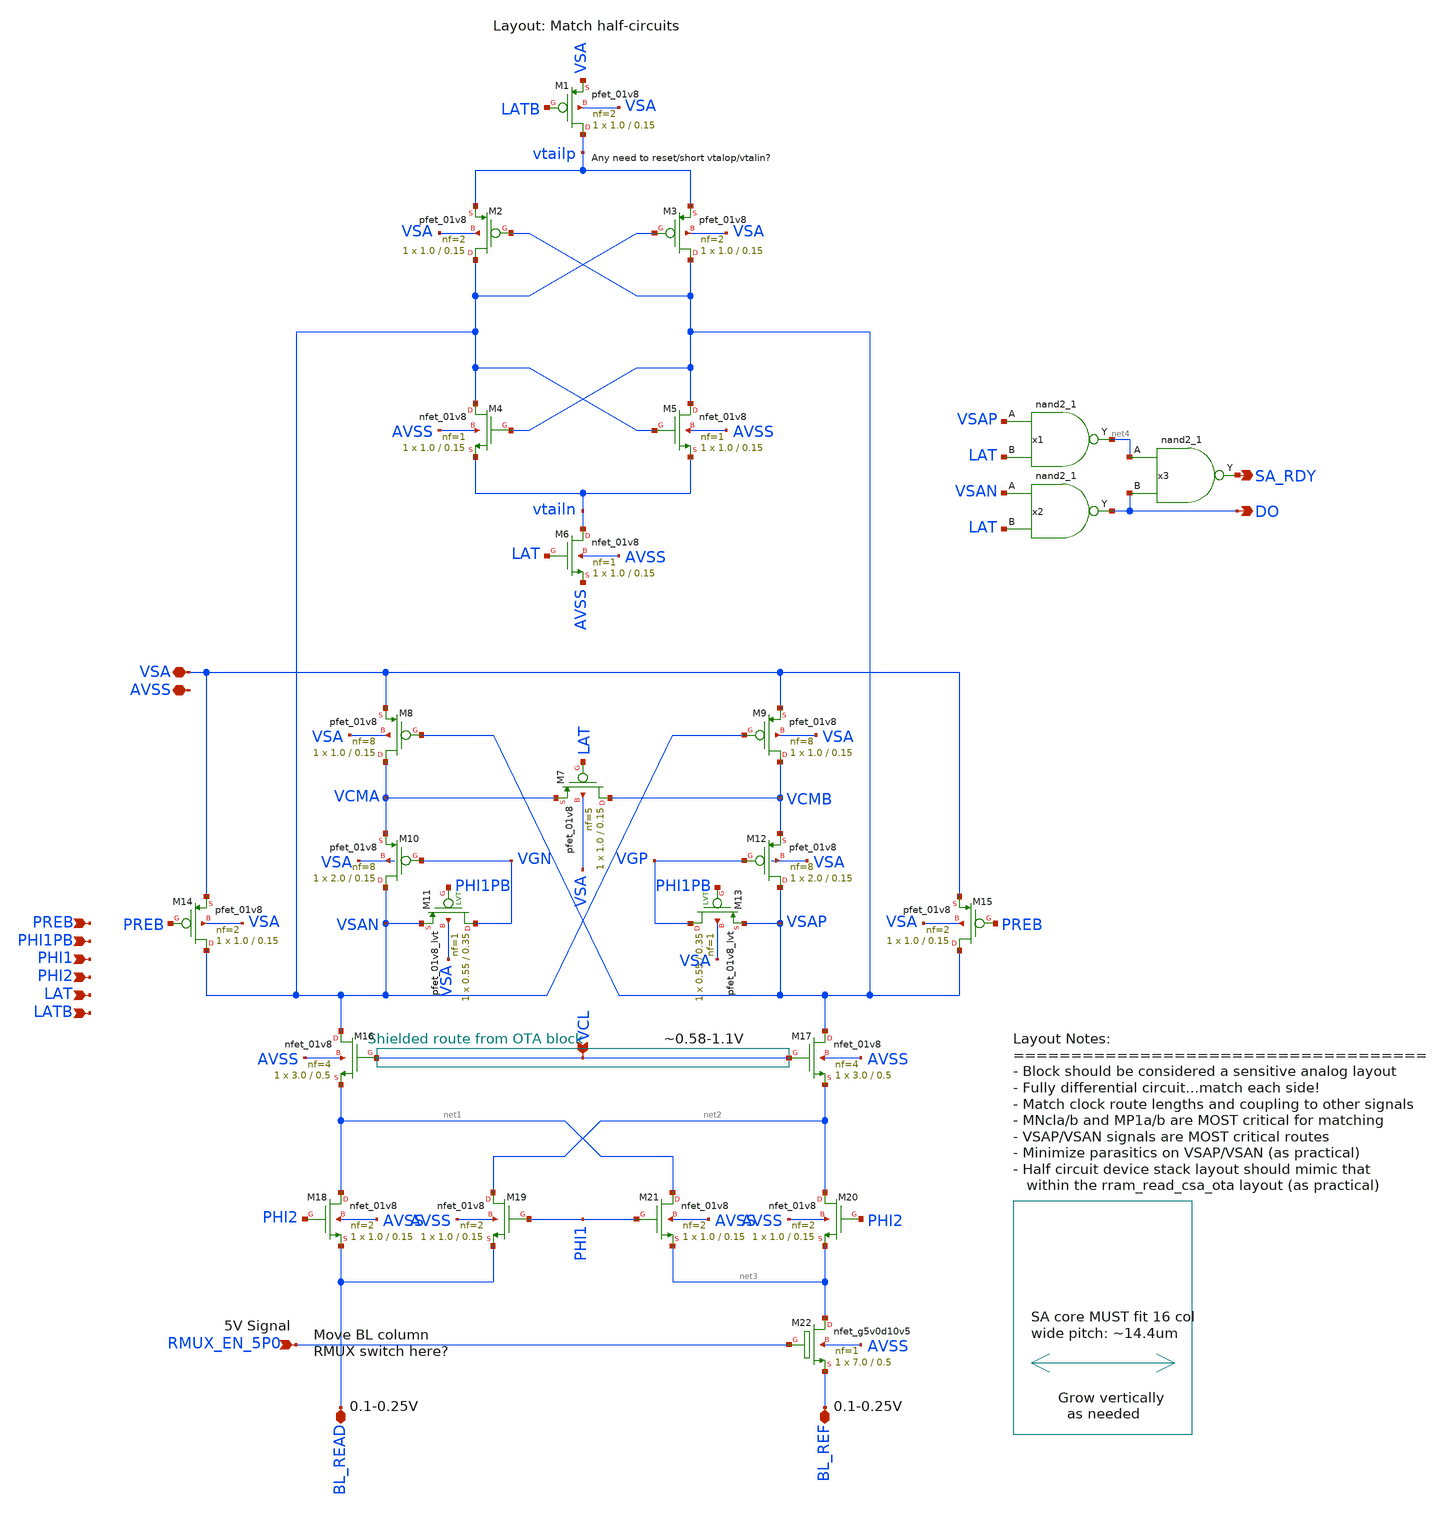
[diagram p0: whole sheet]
** sch_path: BL_Read_Interface/rram_read_csa_core.sch
**.subckt rram_read_csa_core VSA VCL RMUX_EN_5P0 BL_REF BL_READ AVSS PREB PHI1PB PHI1 PHI2 LAT LATB
*+ SA_RDY DO
*.iopin VSA
*.ipin VCL
*.ipin RMUX_EN_5P0
*.iopin BL_REF
*.iopin BL_READ
*.iopin AVSS
*.ipin PREB
*.ipin PHI1PB
*.ipin PHI1
*.ipin PHI2
*.ipin LAT
*.ipin LATB
*.opin SA_RDY
*.opin DO
XM1 vtailp LATB VSA VSA sky130_fd_pr__pfet_01v8 L=0.15 W=1.0 nf=2 ad='int((nf+1)/2) * W/nf * 0.29' as='int((nf+2)/2) * W/nf * 0.29'
+ pd='2*int((nf+1)/2) * (W/nf + 0.29)' ps='2*int((nf+2)/2) * (W/nf + 0.29)' nrd='0.29 / W' nrs='0.29 / W'
+ sa=0 sb=0 sd=0 mult=1 m=1
XM2 VSAN VSAP vtailp VSA sky130_fd_pr__pfet_01v8 L=0.15 W=1.0 nf=2 ad='int((nf+1)/2) * W/nf * 0.29' as='int((nf+2)/2) * W/nf * 0.29'
+ pd='2*int((nf+1)/2) * (W/nf + 0.29)' ps='2*int((nf+2)/2) * (W/nf + 0.29)' nrd='0.29 / W' nrs='0.29 / W'
+ sa=0 sb=0 sd=0 mult=1 m=1
XM3 VSAP VSAN vtailp VSA sky130_fd_pr__pfet_01v8 L=0.15 W=1.0 nf=2 ad='int((nf+1)/2) * W/nf * 0.29' as='int((nf+2)/2) * W/nf * 0.29'
+ pd='2*int((nf+1)/2) * (W/nf + 0.29)' ps='2*int((nf+2)/2) * (W/nf + 0.29)' nrd='0.29 / W' nrs='0.29 / W'
+ sa=0 sb=0 sd=0 mult=1 m=1
XM4 VSAN VSAP vtailn AVSS sky130_fd_pr__nfet_01v8 L=0.15 W=1.0 nf=1 ad='int((nf+1)/2) * W/nf * 0.29'
+ as='int((nf+2)/2) * W/nf * 0.29' pd='2*int((nf+1)/2) * (W/nf + 0.29)' ps='2*int((nf+2)/2) * (W/nf + 0.29)'
+ nrd='0.29 / W' nrs='0.29 / W' sa=0 sb=0 sd=0 mult=1 m=1
XM5 VSAP VSAN vtailn AVSS sky130_fd_pr__nfet_01v8 L=0.15 W=1.0 nf=1 ad='int((nf+1)/2) * W/nf * 0.29'
+ as='int((nf+2)/2) * W/nf * 0.29' pd='2*int((nf+1)/2) * (W/nf + 0.29)' ps='2*int((nf+2)/2) * (W/nf + 0.29)'
+ nrd='0.29 / W' nrs='0.29 / W' sa=0 sb=0 sd=0 mult=1 m=1
XM6 vtailn LAT AVSS AVSS sky130_fd_pr__nfet_01v8 L=0.15 W=1.0 nf=1 ad='int((nf+1)/2) * W/nf * 0.29' as='int((nf+2)/2) * W/nf * 0.29'
+ pd='2*int((nf+1)/2) * (W/nf + 0.29)' ps='2*int((nf+2)/2) * (W/nf + 0.29)' nrd='0.29 / W' nrs='0.29 / W'
+ sa=0 sb=0 sd=0 mult=1 m=1
XM7 VCMB LAT VCMA VSA sky130_fd_pr__pfet_01v8 L=0.15 W=1.0 nf=5 ad='int((nf+1)/2) * W/nf * 0.29' as='int((nf+2)/2) * W/nf * 0.29'
+ pd='2*int((nf+1)/2) * (W/nf + 0.29)' ps='2*int((nf+2)/2) * (W/nf + 0.29)' nrd='0.29 / W' nrs='0.29 / W'
+ sa=0 sb=0 sd=0 mult=1 m=1
XM8 VCMA VSAP VSA VSA sky130_fd_pr__pfet_01v8 L=0.15 W=1.0 nf=8 ad='int((nf+1)/2) * W/nf * 0.29' as='int((nf+2)/2) * W/nf * 0.29'
+ pd='2*int((nf+1)/2) * (W/nf + 0.29)' ps='2*int((nf+2)/2) * (W/nf + 0.29)' nrd='0.29 / W' nrs='0.29 / W'
+ sa=0 sb=0 sd=0 mult=1 m=1
XM9 VCMB VSAN VSA VSA sky130_fd_pr__pfet_01v8 L=0.15 W=1.0 nf=8 ad='int((nf+1)/2) * W/nf * 0.29' as='int((nf+2)/2) * W/nf * 0.29'
+ pd='2*int((nf+1)/2) * (W/nf + 0.29)' ps='2*int((nf+2)/2) * (W/nf + 0.29)' nrd='0.29 / W' nrs='0.29 / W'
+ sa=0 sb=0 sd=0 mult=1 m=1
XM10 VSAN VGN VCMA VSA sky130_fd_pr__pfet_01v8 L=0.15 W=2.0 nf=8 ad='int((nf+1)/2) * W/nf * 0.29' as='int((nf+2)/2) * W/nf * 0.29'
+ pd='2*int((nf+1)/2) * (W/nf + 0.29)' ps='2*int((nf+2)/2) * (W/nf + 0.29)' nrd='0.29 / W' nrs='0.29 / W'
+ sa=0 sb=0 sd=0 mult=1 m=1
XM11 VGN PHI1PB VSAN VSA sky130_fd_pr__pfet_01v8_lvt L=0.35 W=0.55 nf=1 ad='int((nf+1)/2) * W/nf * 0.29'
+ as='int((nf+2)/2) * W/nf * 0.29' pd='2*int((nf+1)/2) * (W/nf + 0.29)' ps='2*int((nf+2)/2) * (W/nf + 0.29)'
+ nrd='0.29 / W' nrs='0.29 / W' sa=0 sb=0 sd=0 mult=1 m=1
XM12 VSAP VGP VCMB VSA sky130_fd_pr__pfet_01v8 L=0.15 W=2.0 nf=8 ad='int((nf+1)/2) * W/nf * 0.29' as='int((nf+2)/2) * W/nf * 0.29'
+ pd='2*int((nf+1)/2) * (W/nf + 0.29)' ps='2*int((nf+2)/2) * (W/nf + 0.29)' nrd='0.29 / W' nrs='0.29 / W'
+ sa=0 sb=0 sd=0 mult=1 m=1
XM13 VGP PHI1PB VSAP VSA sky130_fd_pr__pfet_01v8_lvt L=0.35 W=0.55 nf=1 ad='int((nf+1)/2) * W/nf * 0.29'
+ as='int((nf+2)/2) * W/nf * 0.29' pd='2*int((nf+1)/2) * (W/nf + 0.29)' ps='2*int((nf+2)/2) * (W/nf + 0.29)'
+ nrd='0.29 / W' nrs='0.29 / W' sa=0 sb=0 sd=0 mult=1 m=1
XM14 VSAN PREB VSA VSA sky130_fd_pr__pfet_01v8 L=0.15 W=1.0 nf=2 ad='int((nf+1)/2) * W/nf * 0.29' as='int((nf+2)/2) * W/nf * 0.29'
+ pd='2*int((nf+1)/2) * (W/nf + 0.29)' ps='2*int((nf+2)/2) * (W/nf + 0.29)' nrd='0.29 / W' nrs='0.29 / W'
+ sa=0 sb=0 sd=0 mult=1 m=1
XM15 VSAP PREB VSA VSA sky130_fd_pr__pfet_01v8 L=0.15 W=1.0 nf=2 ad='int((nf+1)/2) * W/nf * 0.29' as='int((nf+2)/2) * W/nf * 0.29'
+ pd='2*int((nf+1)/2) * (W/nf + 0.29)' ps='2*int((nf+2)/2) * (W/nf + 0.29)' nrd='0.29 / W' nrs='0.29 / W'
+ sa=0 sb=0 sd=0 mult=1 m=1
XM16 VSAN VCL net1 AVSS sky130_fd_pr__nfet_01v8 L=0.5 W=3.0 nf=4 ad='int((nf+1)/2) * W/nf * 0.29' as='int((nf+2)/2) * W/nf * 0.29'
+ pd='2*int((nf+1)/2) * (W/nf + 0.29)' ps='2*int((nf+2)/2) * (W/nf + 0.29)' nrd='0.29 / W' nrs='0.29 / W'
+ sa=0 sb=0 sd=0 mult=1 m=1
XM17 VSAP VCL net2 AVSS sky130_fd_pr__nfet_01v8 L=0.5 W=3.0 nf=4 ad='int((nf+1)/2) * W/nf * 0.29' as='int((nf+2)/2) * W/nf * 0.29'
+ pd='2*int((nf+1)/2) * (W/nf + 0.29)' ps='2*int((nf+2)/2) * (W/nf + 0.29)' nrd='0.29 / W' nrs='0.29 / W'
+ sa=0 sb=0 sd=0 mult=1 m=1
XM18 net1 PHI2 BL_READ AVSS sky130_fd_pr__nfet_01v8 L=0.15 W=1.0 nf=2 ad='int((nf+1)/2) * W/nf * 0.29'
+ as='int((nf+2)/2) * W/nf * 0.29' pd='2*int((nf+1)/2) * (W/nf + 0.29)' ps='2*int((nf+2)/2) * (W/nf + 0.29)'
+ nrd='0.29 / W' nrs='0.29 / W' sa=0 sb=0 sd=0 mult=1 m=1
XM19 net2 PHI1 BL_READ AVSS sky130_fd_pr__nfet_01v8 L=0.15 W=1.0 nf=2 ad='int((nf+1)/2) * W/nf * 0.29'
+ as='int((nf+2)/2) * W/nf * 0.29' pd='2*int((nf+1)/2) * (W/nf + 0.29)' ps='2*int((nf+2)/2) * (W/nf + 0.29)'
+ nrd='0.29 / W' nrs='0.29 / W' sa=0 sb=0 sd=0 mult=1 m=1
XM20 net2 PHI2 net3 AVSS sky130_fd_pr__nfet_01v8 L=0.15 W=1.0 nf=2 ad='int((nf+1)/2) * W/nf * 0.29' as='int((nf+2)/2) * W/nf * 0.29'
+ pd='2*int((nf+1)/2) * (W/nf + 0.29)' ps='2*int((nf+2)/2) * (W/nf + 0.29)' nrd='0.29 / W' nrs='0.29 / W'
+ sa=0 sb=0 sd=0 mult=1 m=1
XM21 net1 PHI1 net3 AVSS sky130_fd_pr__nfet_01v8 L=0.15 W=1.0 nf=2 ad='int((nf+1)/2) * W/nf * 0.29' as='int((nf+2)/2) * W/nf * 0.29'
+ pd='2*int((nf+1)/2) * (W/nf + 0.29)' ps='2*int((nf+2)/2) * (W/nf + 0.29)' nrd='0.29 / W' nrs='0.29 / W'
+ sa=0 sb=0 sd=0 mult=1 m=1
XM22 net3 RMUX_EN_5P0 BL_REF AVSS sky130_fd_pr__nfet_g5v0d10v5 L=0.5 W=7.0 nf=1 ad='int((nf+1)/2) * W/nf * 0.29'
+ as='int((nf+2)/2) * W/nf * 0.29' pd='2*int((nf+1)/2) * (W/nf + 0.29)' ps='2*int((nf+2)/2) * (W/nf + 0.29)'
+ nrd='0.29 / W' nrs='0.29 / W' sa=0 sb=0 sd=0 mult=1 m=1
x1 VSAP LAT AVSS AVSS VSA VSA net4 sky130_fd_sc_hd__nand2_1
x2 VSAN LAT AVSS AVSS VSA VSA DO sky130_fd_sc_hd__nand2_1
x3 net4 DO AVSS AVSS VSA VSA SA_RDY sky130_fd_sc_hd__nand2_1
**.ends
.end
